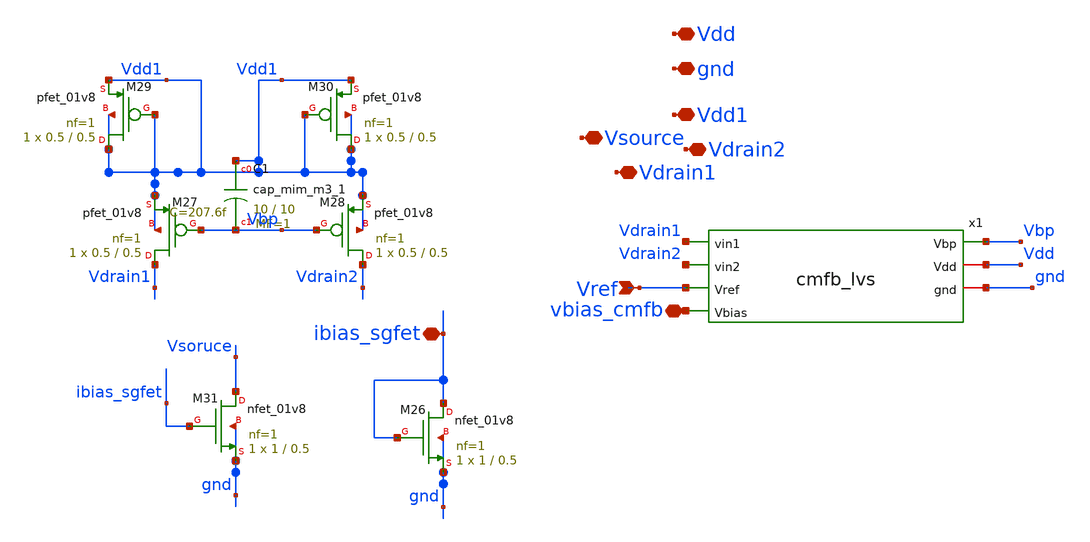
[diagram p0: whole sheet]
** sch_path: xschem/first_stage_differential_amp.sch
**.subckt first_stage_differential_amp gnd Vdd Vref ibias_sgfet vbias_cmfb Vdd1 Vsource Vdrain1
*+ Vdrain2
*.iopin gnd
*.iopin Vdd
*.ipin Vref
*.iopin ibias_sgfet
*.iopin vbias_cmfb
*.iopin Vdd1
*.iopin Vsource
*.iopin Vdrain1
*.iopin Vdrain2
x1 Vbp Vdd gnd Vdrain1 Vdrain2 Vref vbias_cmfb cmfb_lvs
XM26 ibias_sgfet ibias_sgfet gnd gnd sky130_fd_pr__nfet_01v8 L=0.5 W=1 nf=1 ad='int((nf+1)/2) * W/nf * 0.29'
+ as='int((nf+2)/2) * W/nf * 0.29' pd='2*int((nf+1)/2) * (W/nf + 0.29)' ps='2*int((nf+2)/2) * (W/nf + 0.29)'
+ nrd='0.29 / W' nrs='0.29 / W' sa=0 sb=0 sd=0 mult=1 m=1
XM27 Vdrain1 Vbp Vdd1 Vdd1 sky130_fd_pr__pfet_01v8 L=0.5 W=0.5 nf=1 ad='int((nf+1)/2) * W/nf * 0.29'
+ as='int((nf+2)/2) * W/nf * 0.29' pd='2*int((nf+1)/2) * (W/nf + 0.29)' ps='2*int((nf+2)/2) * (W/nf + 0.29)'
+ nrd='0.29 / W' nrs='0.29 / W' sa=0 sb=0 sd=0 mult=1 m=1
XM28 Vdrain2 Vbp Vdd1 Vdd1 sky130_fd_pr__pfet_01v8 L=0.5 W=0.5 nf=1 ad='int((nf+1)/2) * W/nf * 0.29'
+ as='int((nf+2)/2) * W/nf * 0.29' pd='2*int((nf+1)/2) * (W/nf + 0.29)' ps='2*int((nf+2)/2) * (W/nf + 0.29)'
+ nrd='0.29 / W' nrs='0.29 / W' sa=0 sb=0 sd=0 mult=1 m=1
XM29 Vdd1 Vdd1 Vdd1 Vdd1 sky130_fd_pr__pfet_01v8 L=0.5 W=0.5 nf=1 ad='int((nf+1)/2) * W/nf * 0.29' as='int((nf+2)/2) * W/nf * 0.29'
+ pd='2*int((nf+1)/2) * (W/nf + 0.29)' ps='2*int((nf+2)/2) * (W/nf + 0.29)' nrd='0.29 / W' nrs='0.29 / W'
+ sa=0 sb=0 sd=0 mult=1 m=1
XM30 Vdd1 Vdd1 Vdd1 Vdd1 sky130_fd_pr__pfet_01v8 L=0.5 W=0.5 nf=1 ad='int((nf+1)/2) * W/nf * 0.29' as='int((nf+2)/2) * W/nf * 0.29'
+ pd='2*int((nf+1)/2) * (W/nf + 0.29)' ps='2*int((nf+2)/2) * (W/nf + 0.29)' nrd='0.29 / W' nrs='0.29 / W'
+ sa=0 sb=0 sd=0 mult=1 m=1
XM31 Vsoruce ibias_sgfet gnd gnd sky130_fd_pr__nfet_01v8 L=0.5 W=1 nf=1 ad='int((nf+1)/2) * W/nf * 0.29'
+ as='int((nf+2)/2) * W/nf * 0.29' pd='2*int((nf+1)/2) * (W/nf + 0.29)' ps='2*int((nf+2)/2) * (W/nf + 0.29)'
+ nrd='0.29 / W' nrs='0.29 / W' sa=0 sb=0 sd=0 mult=1 m=1
XC1 Vdd1 Vbp sky130_fd_pr__cap_mim_m3_1 W=10 L=10 MF=1 m=1
**.ends
.end
